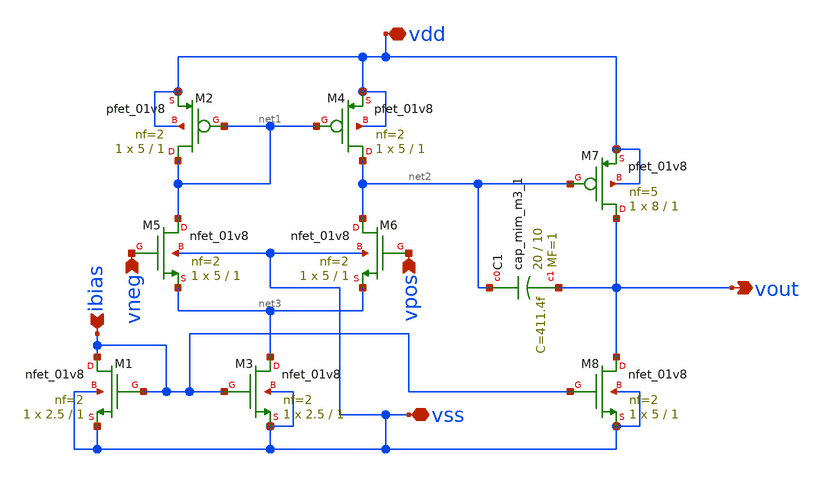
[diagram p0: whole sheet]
** sch_path: sch/opamp6.sch
**.subckt opamp6 ibias vneg vpos vout vdd vss
*.ipin ibias
*.ipin vneg
*.ipin vpos
*.opin vout
*.iopin vdd
*.iopin vss
XM1 ibias ibias vss vss sky130_fd_pr__nfet_01v8 L=1 W=2.5 nf=2 ad='int((2 + 1)/2) * 2.5 / 2 * 0.29' as='int((2 + 2)/2) * 2.5 / 2 * 0.29'
+ pd='2*int((2 + 1)/2) * (2.5 / 2 + 0.29)' ps='2*int((2 + 2)/2) * (2.5 / 2 + 0.29)' nrd='0.29 / 2.5 ' nrs='0.29 / 2.5 '
+ sa=0 sb=0 sd=0 mult=1 m=1
XM2 net1 net1 vdd vdd sky130_fd_pr__pfet_01v8 L=1 W=5 nf=2 ad='int((2 + 1)/2) * 5 / 2 * 0.29' as='int((2 + 2)/2) * 5 / 2 * 0.29'
+ pd='2*int((2 + 1)/2) * (5 / 2 + 0.29)' ps='2*int((2 + 2)/2) * (5 / 2 + 0.29)' nrd='0.29 / 5 ' nrs='0.29 / 5 '
+ sa=0 sb=0 sd=0 mult=1 m=1
XM3 net3 ibias vss vss sky130_fd_pr__nfet_01v8 L=1 W=2.5 nf=2 ad='int((2 + 1)/2) * 2.5 / 2 * 0.29' as='int((2 + 2)/2) * 2.5 / 2 * 0.29'
+ pd='2*int((2 + 1)/2) * (2.5 / 2 + 0.29)' ps='2*int((2 + 2)/2) * (2.5 / 2 + 0.29)' nrd='0.29 / 2.5 ' nrs='0.29 / 2.5 '
+ sa=0 sb=0 sd=0 mult=1 m=1
XM4 net2 net1 vdd vdd sky130_fd_pr__pfet_01v8 L=1 W=5 nf=2 ad='int((2 + 1)/2) * 5 / 2 * 0.29' as='int((2 + 2)/2) * 5 / 2 * 0.29'
+ pd='2*int((2 + 1)/2) * (5 / 2 + 0.29)' ps='2*int((2 + 2)/2) * (5 / 2 + 0.29)' nrd='0.29 / 5 ' nrs='0.29 / 5 '
+ sa=0 sb=0 sd=0 mult=1 m=1
XM5 net1 vneg net3 vss sky130_fd_pr__nfet_01v8 L=1 W=5 nf=2 ad='int((2 + 1)/2) * 5 / 2 * 0.29' as='int((2 + 2)/2) * 5 / 2 * 0.29'
+ pd='2*int((2 + 1)/2) * (5 / 2 + 0.29)' ps='2*int((2 + 2)/2) * (5 / 2 + 0.29)' nrd='0.29 / 5 ' nrs='0.29 / 5 '
+ sa=0 sb=0 sd=0 mult=1 m=1
XM6 net2 vpos net3 vss sky130_fd_pr__nfet_01v8 L=1 W=5 nf=2 ad='int((2 + 1)/2) * 5 / 2 * 0.29' as='int((2 + 2)/2) * 5 / 2 * 0.29'
+ pd='2*int((2 + 1)/2) * (5 / 2 + 0.29)' ps='2*int((2 + 2)/2) * (5 / 2 + 0.29)' nrd='0.29 / 5 ' nrs='0.29 / 5 '
+ sa=0 sb=0 sd=0 mult=1 m=1
XM7 vout net2 vdd vdd sky130_fd_pr__pfet_01v8 L=1 W=8 nf=5 ad='int((5 + 1)/2) * 8 / 5 * 0.29' as='int((5 + 2)/2) * 8 / 5 * 0.29'
+ pd='2*int((5 + 1)/2) * (8 / 5 + 0.29)' ps='2*int((5 + 2)/2) * (8 / 5 + 0.29)' nrd='0.29 / 8 ' nrs='0.29 / 8 '
+ sa=0 sb=0 sd=0 mult=1 m=1
XM8 vout ibias vss vss sky130_fd_pr__nfet_01v8 L=1 W=5 nf=2 ad='int((2 + 1)/2) * 5 / 2 * 0.29' as='int((2 + 2)/2) * 5 / 2 * 0.29'
+ pd='2*int((2 + 1)/2) * (5 / 2 + 0.29)' ps='2*int((2 + 2)/2) * (5 / 2 + 0.29)' nrd='0.29 / 5 ' nrs='0.29 / 5 '
+ sa=0 sb=0 sd=0 mult=1 m=1
XC1 net2 vout sky130_fd_pr__cap_mim_m3_1 W=20 L=10 MF=1 m=1
**.ends
.end
